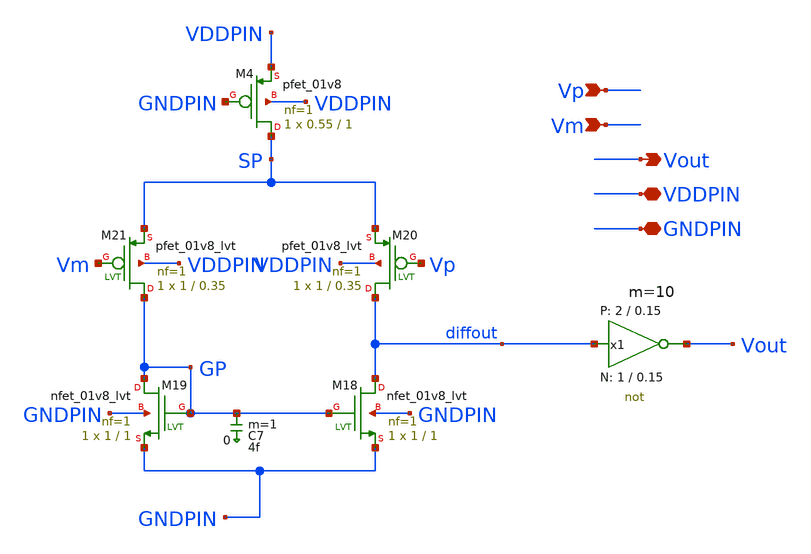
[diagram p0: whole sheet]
** sch_path: simpleComp.sch
* StefanSchippers/xschem_sky130/sky130_tests/not.sch:
* Copyright 2021 Stefan Frederik Schippers
* Licensed under the Apache License, Version 2.0 (the "License");
**.subckt simpleComp Vp Vm Vout VDDPIN GNDPIN
*.ipin Vp
*.ipin Vm
*.opin Vout
*.iopin VDDPIN
*.iopin GNDPIN
C7 GP 0 4f m=1
XM4 SP GNDPIN VDDPIN VDDPIN sky130_fd_pr__pfet_01v8 L=1 W=0.55 nf=1 ad='W * 0.29' as='W * 0.29' pd='W + 2 * 0.29'
+ ps='W + 2 * 0.29' nrd=0 nrs=0 sa=0 sb=0 sd=0 mult=1 m=1
XM18 diffout GP GNDPIN GNDPIN sky130_fd_pr__nfet_01v8_lvt L=1 W=1 nf=1 ad='W * 0.29' as='W * 0.29' pd='2*(W + 0.29)'
+ ps='2*(W + 0.29)' nrd=0 nrs=0 sa=0 sb=0 sd=0 mult=1 m=1
XM19 GP GP GNDPIN GNDPIN sky130_fd_pr__nfet_01v8_lvt L=1 W=1 nf=1 ad='W * 0.29' as='W * 0.29' pd='2*(W + 0.29)'
+ ps='2*(W + 0.29)' nrd=0 nrs=0 sa=0 sb=0 sd=0 mult=1 m=1
XM20 diffout Vp SP VDDPIN sky130_fd_pr__pfet_01v8_lvt L=0.35 W=1 nf=1 ad='W * 0.29' as='W * 0.29' pd='2*(W + 0.29)'
+ ps='2*(W + 0.29)' nrd=0 nrs=0 sa=0 sb=0 sd=0 mult=1 m=1
XM21 GP Vm SP VDDPIN sky130_fd_pr__pfet_01v8_lvt L=0.35 W=1 nf=1 ad='W * 0.29' as='W * 0.29' pd='2*(W + 0.29)'
+ ps='2*(W + 0.29)' nrd=0 nrs=0 sa=0 sb=0 sd=0 mult=1 m=1
x1 Vout diffout VDDPIN GNDPIN not W_N=1 L_N=0.15 W_P=2 L_P=0.15 m=10
**.ends

* expanding   symbol:  not.sym # of pins=2
** sym_path: not.sym
** sch_path: not.sch
.subckt not y a VCCPIN VSSPIN     W_N=1 L_N=0.15 W_P=2 L_P=0.15
*.opin y
*.ipin a
XM1 DN a VSSPIN VSSPIN sky130_fd_pr__nfet_01v8 L=L_N W=W_N nf=1 ad='int((1 + 1)/2) * W_N / 1 * 0.29'
+ as='int((1 + 2)/2) * W_N / 1 * 0.29' pd='2*int((1 + 1)/2) * (W_N / 1 + 0.29)' ps='2*int((1 + 2)/2) * (W_N / 1 + 0.29)'
+ nrd='0.29 / W_N ' nrs='0.29 / W_N ' sa=0 sb=0 sd=0 mult=1 m=1
XM2 DP a VCCPIN VCCPIN sky130_fd_pr__pfet_01v8 L=L_P W=W_P nf=1 ad='int((nf+1)/2) * W/nf * 0.29' as='int((nf+2)/2) * W/nf * 0.29'
+ pd='2*int((nf+1)/2) * (W/nf + 0.29)' ps='2*int((nf+2)/2) * (W/nf + 0.29)' nrd='0.29 / W' nrs='0.29 / W'
+ sa=0 sb=0 sd=0 mult=1 m=1
Vmeas DP y 0
.save i(vmeas)
Vmeas1 y DN 0
.save i(vmeas1)
.save v(dp)
.save v(dn)
.ends

.end
